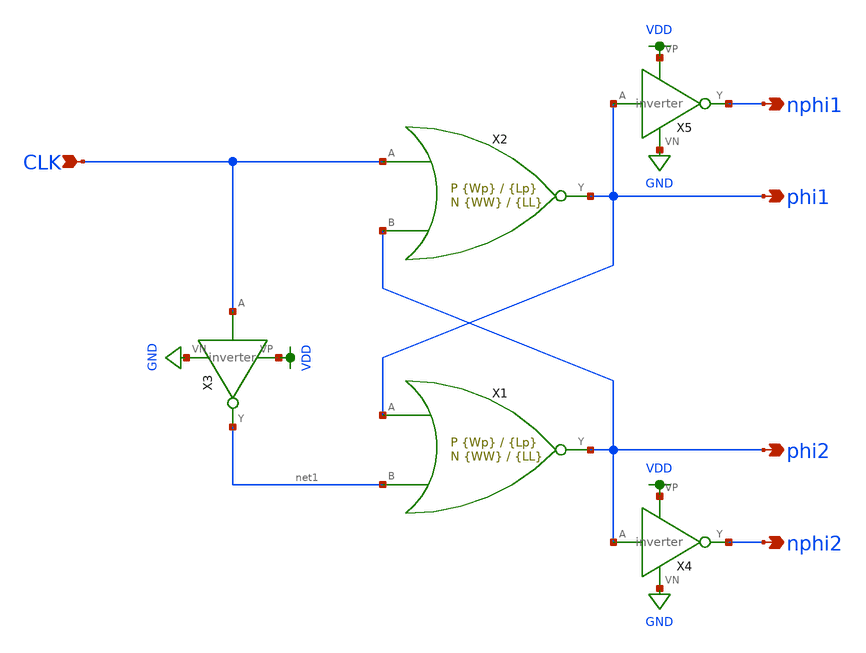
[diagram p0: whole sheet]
** sch_path: schematic/clk_gen.sch
**.subckt clk_gen phi1 nphi1 nphi2 phi2 CLK
*.opin phi1
*.opin nphi1
*.opin nphi2
*.opin phi2
*.ipin CLK
X3 CLK net1 VDD GND inverter
X4 phi2 nphi2 VDD GND inverter
X5 phi1 nphi1 VDD GND inverter
X1 phi1 phi2 net1 nor2 Wp={Wp} Lp={Lp} WW={WW} LL={LL}
X2 CLK phi1 phi2 nor2 Wp={Wp} Lp={Lp} WW={WW} LL={LL}
**.ends

* expanding   symbol:  /home/madvlsi/Documents/MADVLSI-Final_Project/schematic/inverter.sym # of
*+ pins=4
** sym_path: schematic/inverter.sym
** sch_path: schematic/inverter.sch
.subckt inverter A Y VP VN
*.opin Y
*.ipin A
*.iopin VP
*.iopin VN
XM3 Y A VP VDD sky130_fd_pr__pfet_01v8 L={Lp} W={Wp} nf=1 ad='int((nf+1)/2) * W/nf * 0.29' as='int((nf+2)/2) * W/nf * 0.29'
+ pd='2*int((nf+1)/2) * (W/nf + 0.29)' ps='2*int((nf+2)/2) * (W/nf + 0.29)' nrd='0.29 / W' nrs='0.29 / W'
+ sa=0 sb=0 sd=0 mult=1 m=1
XM4 Y A VP VDD sky130_fd_pr__pfet_01v8 L={Lp} W={Wp} nf=1 ad='int((nf+1)/2) * W/nf * 0.29' as='int((nf+2)/2) * W/nf * 0.29'
+ pd='2*int((nf+1)/2) * (W/nf + 0.29)' ps='2*int((nf+2)/2) * (W/nf + 0.29)' nrd='0.29 / W' nrs='0.29 / W'
+ sa=0 sb=0 sd=0 mult=1 m=1
XM5 Y A VN GND sky130_fd_pr__nfet_01v8 L={Lp} W={Wp} nf=1 ad='int((nf+1)/2) * W/nf * 0.29' as='int((nf+2)/2) * W/nf * 0.29'
+ pd='2*int((nf+1)/2) * (W/nf + 0.29)' ps='2*int((nf+2)/2) * (W/nf + 0.29)' nrd='0.29 / W' nrs='0.29 / W'
+ sa=0 sb=0 sd=0 mult=1 m=1
.ends


* expanding   symbol:  /home/madvlsi/Documents/MADVLSI-Final_Project/schematic/nor2.sym # of pins=3
** sym_path: schematic/nor2.sym
** sch_path: schematic/nor2.sch
.subckt nor2 A Y B  Wp=1 Lp=0.15 WW=1 LL=0.15
*.ipin A
*.ipin B
*.opin Y
XM1 Y A GND GND sky130_fd_pr__nfet_01v8 L={LL} W={WW} nf=1 ad='int((nf+1)/2) * W/nf * 0.29' as='int((nf+2)/2) * W/nf * 0.29'
+ pd='2*int((nf+1)/2) * (W/nf + 0.29)' ps='2*int((nf+2)/2) * (W/nf + 0.29)' nrd='0.29 / W' nrs='0.29 / W'
+ sa=0 sb=0 sd=0 mult=1 m=1
XM2 Y A net1 VDD sky130_fd_pr__pfet_01v8 L={Lp} W={Wp} nf=1 ad='int((nf+1)/2) * W/nf * 0.29' as='int((nf+2)/2) * W/nf * 0.29'
+ pd='2*int((nf+1)/2) * (W/nf + 0.29)' ps='2*int((nf+2)/2) * (W/nf + 0.29)' nrd='0.29 / W' nrs='0.29 / W'
+ sa=0 sb=0 sd=0 mult=1 m=1
XM3 net1 B VDD VDD sky130_fd_pr__pfet_01v8 L={Lp} W={Wp} nf=1 ad='int((nf+1)/2) * W/nf * 0.29' as='int((nf+2)/2) * W/nf * 0.29'
+ pd='2*int((nf+1)/2) * (W/nf + 0.29)' ps='2*int((nf+2)/2) * (W/nf + 0.29)' nrd='0.29 / W' nrs='0.29 / W'
+ sa=0 sb=0 sd=0 mult=1 m=1
XM4 GND B Y GND sky130_fd_pr__nfet_01v8 L={LL} W={WW} nf=1 ad='int((nf+1)/2) * W/nf * 0.29' as='int((nf+2)/2) * W/nf * 0.29'
+ pd='2*int((nf+1)/2) * (W/nf + 0.29)' ps='2*int((nf+2)/2) * (W/nf + 0.29)' nrd='0.29 / W' nrs='0.29 / W'
+ sa=0 sb=0 sd=0 mult=1 m=1
.ends

.GLOBAL VDD
.GLOBAL GND
.end
